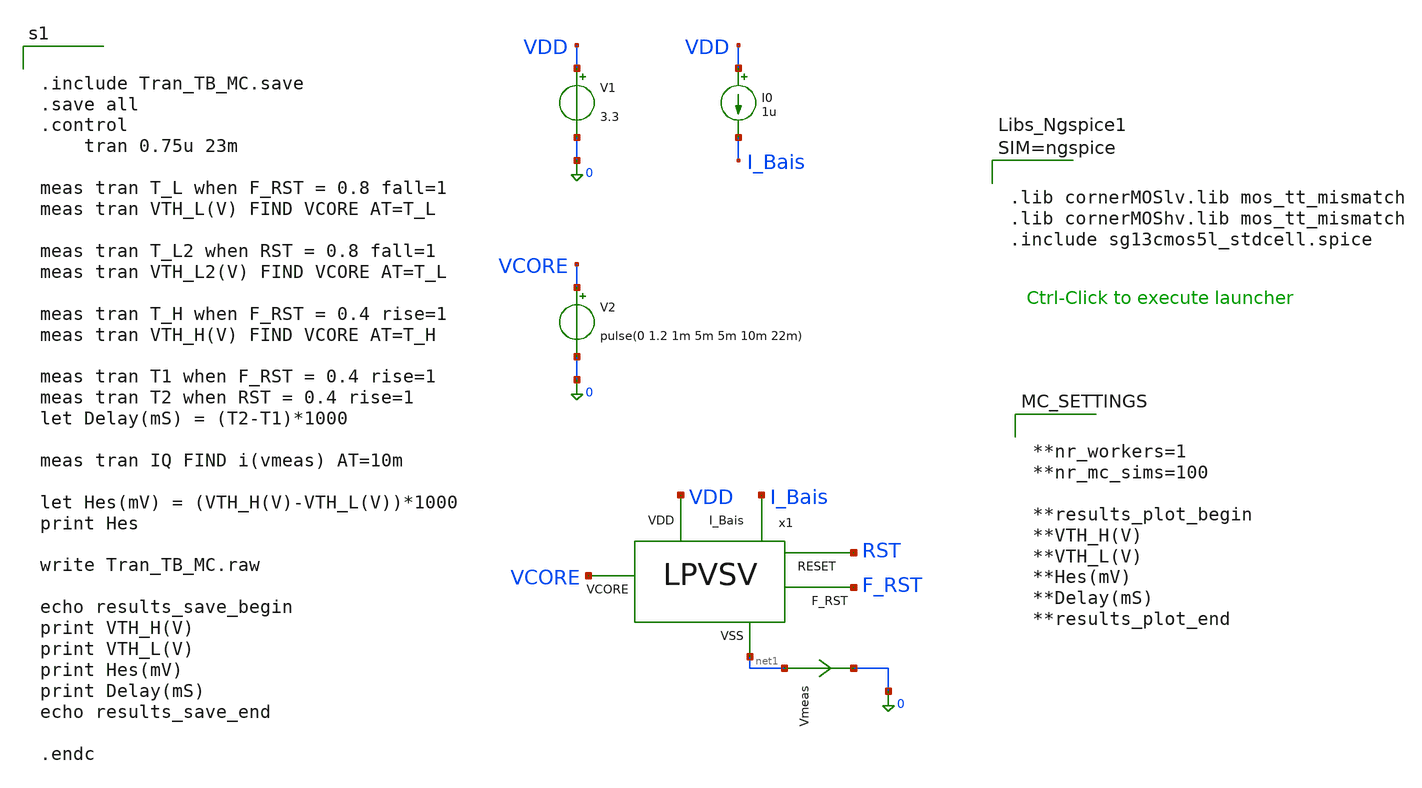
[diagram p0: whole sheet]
** sch_path: Simulation/Tran_Analysis/Tran_TB_MC.sch
**.subckt Tran_TB_MC
x1 VDD VCORE I_Bais RST F_RST net1 LPVSV
I0 VDD I_Bais 1u
V1 VDD 0 3.3
V2 VCORE 0 pulse(0 1.2 1m 5m 5m 10m 22m)
Vmeas net1 0 0
.save i(vmeas)
**** begin user architecture code



.lib cornerMOSlv.lib mos_tt_mismatch
.lib cornerMOShv.lib mos_tt_mismatch
.include sg13cmos5l_stdcell.spice





**nr_workers=1
**nr_mc_sims=100

**results_plot_begin
**VTH_H(V)
**VTH_L(V)
**Hes(mV)
**Delay(mS)
**results_plot_end




.include Tran_TB_MC.save
.save all
.control
	tran 0.75u 23m

meas tran T_L when F_RST = 0.8 fall=1
meas tran VTH_L(V) FIND VCORE AT=T_L

meas tran T_L2 when RST = 0.8 fall=1
meas tran VTH_L2(V) FIND VCORE AT=T_L

meas tran T_H when F_RST = 0.4 rise=1
meas tran VTH_H(V) FIND VCORE AT=T_H

meas tran T1 when F_RST = 0.4 rise=1
meas tran T2 when RST = 0.4 rise=1
let Delay(mS) = (T2-T1)*1000

meas tran IQ FIND i(vmeas) AT=10m

let Hes(mV) = (VTH_H(V)-VTH_L(V))*1000
print Hes

write Tran_TB_MC.raw

echo results_save_begin
print VTH_H(V)
print VTH_L(V)
print Hes(mV)
print Delay(mS)
echo results_save_end

.endc


**** end user architecture code
**.ends
.end
